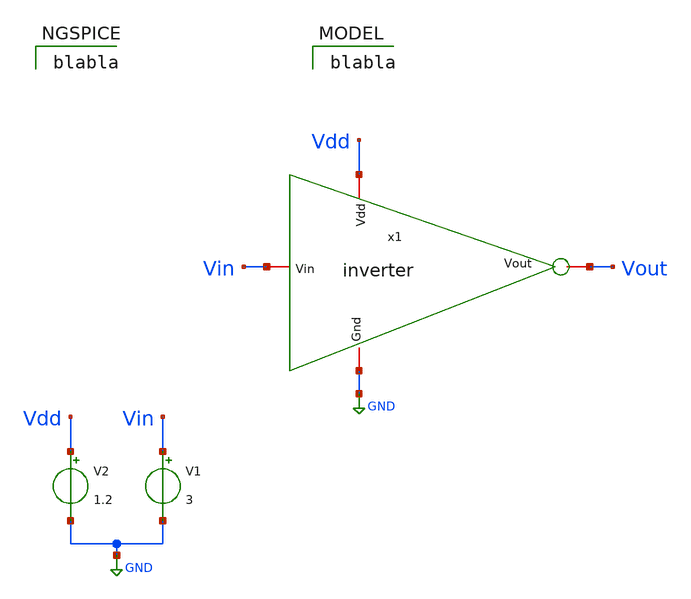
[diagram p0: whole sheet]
** sch_path: tests/data/_invcheck/tb.sch
**.subckt tb
V1 Vin GND 3
V2 Vdd GND 1.2
**** begin user architecture code

blabla

 value=
**** end user architecture code
**.ends
.GLOBAL GND
.end
